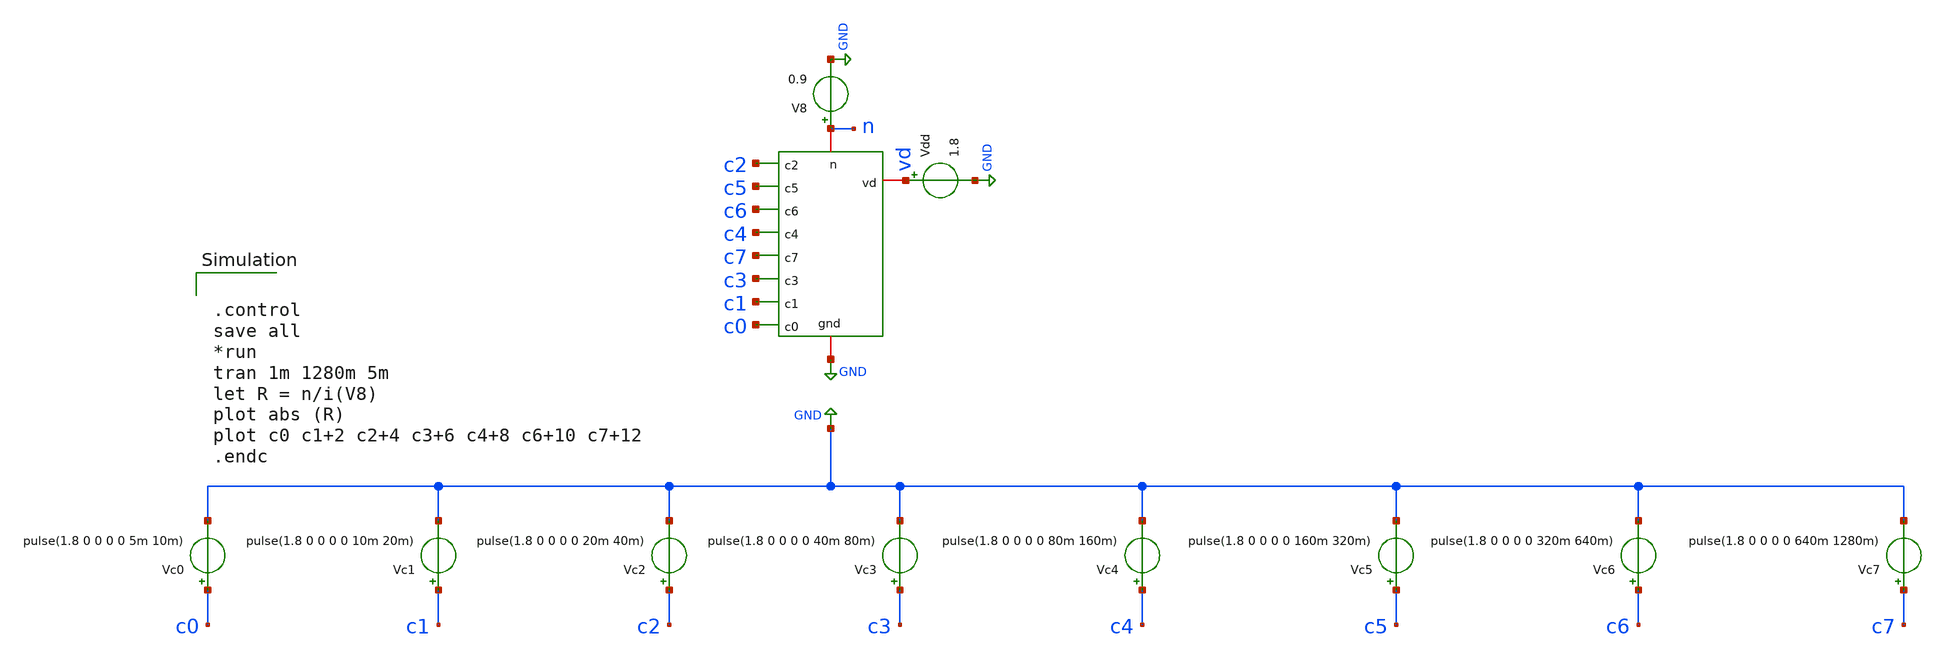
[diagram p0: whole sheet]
** sch_path: .Trash-1000/files/testdp.sch
**.subckt testdp
V8 n GND 0.9
Vdd vd GND 1.8
Vc0 c0 GND pulse(1.8 0 0 0 0 5m 10m)
Vc1 c1 GND pulse(1.8 0 0 0 0 10m 20m)
Vc2 c2 GND pulse(1.8 0 0 0 0 20m 40m)
Vc3 c3 GND pulse(1.8 0 0 0 0 40m 80m)
Vc4 c4 GND pulse(1.8 0 0 0 0 80m 160m)
Vc5 c5 GND pulse(1.8 0 0 0 0 160m 320m)
Vc6 c6 GND pulse(1.8 0 0 0 0 320m 640m)
Vc7 c7 GND pulse(1.8 0 0 0 0 640m 1280m)
x1 n GND vd c2 c5 c6 c4 c7 c3 c1 c0 digipot
**** begin user architecture code


.control
save all
*run
tran 1m 1280m 5m
let R = n/i(V8)
plot abs (R)
plot c0 c1+2 c2+4 c3+6 c4+8 c6+10 c7+12
.endc


** opencircuitdesign pdks install
.lib $::SKYWATER_MODELS/sky130.lib.spice tt_mm


**** end user architecture code
**.ends

* expanding   symbol:  /foss/designs/digipot.sym # of pins=11
** sym_path: xschem/digipot.sym
** sch_path: xschem/digipot.sch
.subckt digipot n gnd vd c2 c5 c6 c4 c7 c3 c1 c0
*.ipin c0
*.ipin c1
*.ipin c2
*.ipin c3
*.ipin c4
*.ipin c5
*.ipin c6
*.ipin c7
*.iopin gnd
*.iopin vd
*.iopin n
x1 vd c0 gnd net1 gnd tg
XR6 net2 n gnd sky130_fd_pr__res_high_po_0p35 L=2.45 mult=1 m=1
x2 vd c1 gnd net3 gnd tg
x3 vd c2 gnd net4 gnd tg
x4 vd c3 gnd net5 gnd tg
x5 vd c4 gnd net6 gnd tg
x6 vd c5 gnd net7 gnd tg
x7 vd c6 gnd net8 gnd tg
x8 vd c7 gnd net2 gnd tg
XR7 net8 n gnd sky130_fd_pr__res_high_po_0p35 L=5.35 mult=1 m=1
XR5 net7 n gnd sky130_fd_pr__res_high_po_0p35 L=11.92 mult=1 m=1
XR4 net6 n gnd sky130_fd_pr__res_high_po_0p35 L=25.05 mult=1 m=1
XR3 net5 n gnd sky130_fd_pr__res_high_po_0p35 L=51.32 mult=1 m=1
XR2 net4 n gnd sky130_fd_pr__res_high_po_0p35 L=103.85 mult=1 m=1
XR1 net3 n gnd sky130_fd_pr__res_high_po_0p35 L=208.92 mult=1 m=1
XR8 net1 n gnd sky130_fd_pr__res_high_po_0p35 L=419.05 mult=1 m=1
.ends


* expanding   symbol:  /foss/designs/tg.sym # of pins=5
** sym_path: xschem/tg.sym
** sch_path: xschem/tg.sch
.subckt tg vd ctrl vgnd A B
*.iopin B
*.iopin A
*.iopin vgnd
*.iopin vd
*.ipin ctrl
x1 vd ctrl nctrl vgnd inverter
XM1 A ctrl B vgnd sky130_fd_pr__nfet_01v8 L=0.15 W=10 nf=1 ad='int((nf+1)/2) * W/nf * 0.29' as='int((nf+2)/2) * W/nf * 0.29'
+ pd='2*int((nf+1)/2) * (W/nf + 0.29)' ps='2*int((nf+2)/2) * (W/nf + 0.29)' nrd='0.29 / W' nrs='0.29 / W'
+ sa=0 sb=0 sd=0 mult=1 m=1
XM2 A nctrl B vd sky130_fd_pr__pfet_01v8 L=0.15 W=30 nf=1 ad='int((nf+1)/2) * W/nf * 0.29' as='int((nf+2)/2) * W/nf * 0.29'
+ pd='2*int((nf+1)/2) * (W/nf + 0.29)' ps='2*int((nf+2)/2) * (W/nf + 0.29)' nrd='0.29 / W' nrs='0.29 / W'
+ sa=0 sb=0 sd=0 mult=1 m=1
.ends


* expanding   symbol:  /foss/designs/inverter/xschem_files/inverter.sym # of pins=4
** sym_path: /foss/designs/inverter/xschem_files/inverter.sym
** sch_path: /foss/designs/inverter/xschem_files/inverter.sch
.subckt inverter vd in out gnd
*.ipin in
*.opin out
*.iopin vd
*.iopin gnd
XN0 out in gnd gnd sky130_fd_pr__nfet_01v8 L=0.15 W=1 nf=1 ad='int((nf+1)/2) * W/nf * 0.29' as='int((nf+2)/2) * W/nf * 0.29'
+ pd='2*int((nf+1)/2) * (W/nf + 0.29)' ps='2*int((nf+2)/2) * (W/nf + 0.29)' nrd='0.29 / W' nrs='0.29 / W'
+ sa=0 sb=0 sd=0 mult=1 m=1
XP0 out in vd vd sky130_fd_pr__pfet_01v8 L=0.15 W=3 nf=1 ad='int((nf+1)/2) * W/nf * 0.29' as='int((nf+2)/2) * W/nf * 0.29'
+ pd='2*int((nf+1)/2) * (W/nf + 0.29)' ps='2*int((nf+2)/2) * (W/nf + 0.29)' nrd='0.29 / W' nrs='0.29 / W'
+ sa=0 sb=0 sd=0 mult=1 m=1
.ends

.GLOBAL GND
.end
